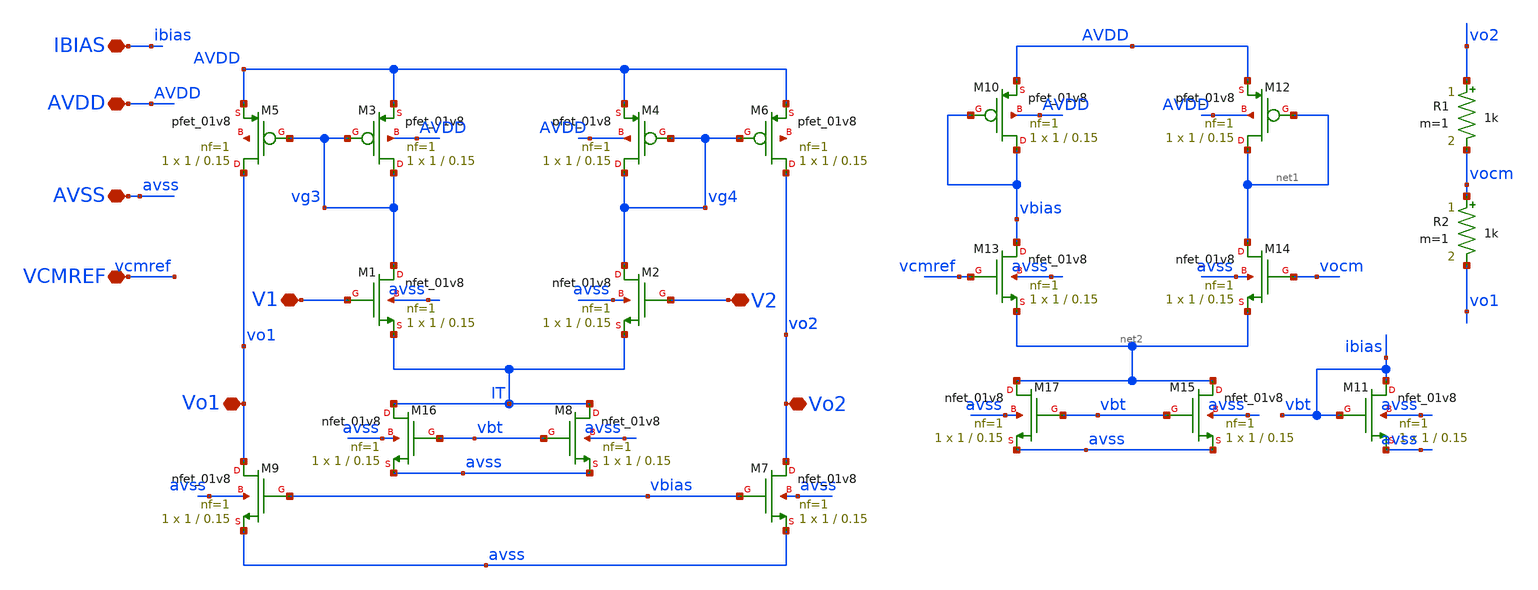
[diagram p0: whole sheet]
** sch_path: xschem/INA/ota_fully_diff.sch
**.subckt ota_fully_diff IBIAS V1 V2 AVDD Vo1 Vo2 AVSS VCMREF
*.iopin IBIAS
*.iopin V1
*.iopin V2
*.iopin AVDD
*.iopin Vo1
*.iopin Vo2
*.iopin AVSS
*.iopin VCMREF
XM3 vg3 vg3 AVDD AVDD sky130_fd_pr__pfet_01v8 L=0.15 W=1 nf=1 ad='int((nf+1)/2) * W/nf * 0.29' as='int((nf+2)/2) * W/nf * 0.29'
+ pd='2*int((nf+1)/2) * (W/nf + 0.29)' ps='2*int((nf+2)/2) * (W/nf + 0.29)' nrd='0.29 / W' nrs='0.29 / W'
+ sa=0 sb=0 sd=0 mult=1 m=1
XM4 vg4 vg4 AVDD AVDD sky130_fd_pr__pfet_01v8 L=0.15 W=1 nf=1 ad='int((nf+1)/2) * W/nf * 0.29' as='int((nf+2)/2) * W/nf * 0.29'
+ pd='2*int((nf+1)/2) * (W/nf + 0.29)' ps='2*int((nf+2)/2) * (W/nf + 0.29)' nrd='0.29 / W' nrs='0.29 / W'
+ sa=0 sb=0 sd=0 mult=1 m=1
XM5 Vo1 vg3 AVDD net3 sky130_fd_pr__pfet_01v8 L=0.15 W=1 nf=1 ad='int((nf+1)/2) * W/nf * 0.29' as='int((nf+2)/2) * W/nf * 0.29'
+ pd='2*int((nf+1)/2) * (W/nf + 0.29)' ps='2*int((nf+2)/2) * (W/nf + 0.29)' nrd='0.29 / W' nrs='0.29 / W'
+ sa=0 sb=0 sd=0 mult=1 m=1
XM6 Vo2 vg4 AVDD net4 sky130_fd_pr__pfet_01v8 L=0.15 W=1 nf=1 ad='int((nf+1)/2) * W/nf * 0.29' as='int((nf+2)/2) * W/nf * 0.29'
+ pd='2*int((nf+1)/2) * (W/nf + 0.29)' ps='2*int((nf+2)/2) * (W/nf + 0.29)' nrd='0.29 / W' nrs='0.29 / W'
+ sa=0 sb=0 sd=0 mult=1 m=1
XM9 Vo1 vbias avss avss sky130_fd_pr__nfet_01v8 L=0.15 W=1 nf=1 ad='int((nf+1)/2) * W/nf * 0.29' as='int((nf+2)/2) * W/nf * 0.29'
+ pd='2*int((nf+1)/2) * (W/nf + 0.29)' ps='2*int((nf+2)/2) * (W/nf + 0.29)' nrd='0.29 / W' nrs='0.29 / W'
+ sa=0 sb=0 sd=0 mult=1 m=1
XM1 vg3 V1 IT avss sky130_fd_pr__nfet_01v8 L=0.15 W=1 nf=1 ad='int((nf+1)/2) * W/nf * 0.29' as='int((nf+2)/2) * W/nf * 0.29'
+ pd='2*int((nf+1)/2) * (W/nf + 0.29)' ps='2*int((nf+2)/2) * (W/nf + 0.29)' nrd='0.29 / W' nrs='0.29 / W'
+ sa=0 sb=0 sd=0 mult=1 m=1
XM2 vg4 V2 IT avss sky130_fd_pr__nfet_01v8 L=0.15 W=1 nf=1 ad='int((nf+1)/2) * W/nf * 0.29' as='int((nf+2)/2) * W/nf * 0.29'
+ pd='2*int((nf+1)/2) * (W/nf + 0.29)' ps='2*int((nf+2)/2) * (W/nf + 0.29)' nrd='0.29 / W' nrs='0.29 / W'
+ sa=0 sb=0 sd=0 mult=1 m=1
XM7 Vo2 vbias avss avss sky130_fd_pr__nfet_01v8 L=0.15 W=1 nf=1 ad='int((nf+1)/2) * W/nf * 0.29' as='int((nf+2)/2) * W/nf * 0.29'
+ pd='2*int((nf+1)/2) * (W/nf + 0.29)' ps='2*int((nf+2)/2) * (W/nf + 0.29)' nrd='0.29 / W' nrs='0.29 / W'
+ sa=0 sb=0 sd=0 mult=1 m=1
XM8 IT vbt avss avss sky130_fd_pr__nfet_01v8 L=0.15 W=1 nf=1 ad='int((nf+1)/2) * W/nf * 0.29' as='int((nf+2)/2) * W/nf * 0.29'
+ pd='2*int((nf+1)/2) * (W/nf + 0.29)' ps='2*int((nf+2)/2) * (W/nf + 0.29)' nrd='0.29 / W' nrs='0.29 / W'
+ sa=0 sb=0 sd=0 mult=1 m=1
XM11 ibias ibias avss avss sky130_fd_pr__nfet_01v8 L=0.15 W=1 nf=1 ad='int((nf+1)/2) * W/nf * 0.29' as='int((nf+2)/2) * W/nf * 0.29'
+ pd='2*int((nf+1)/2) * (W/nf + 0.29)' ps='2*int((nf+2)/2) * (W/nf + 0.29)' nrd='0.29 / W' nrs='0.29 / W'
+ sa=0 sb=0 sd=0 mult=1 m=1
R1 vo2 vocm 1k m=1
R2 vocm vo1 1k m=1
XM10 vbias vbias AVDD AVDD sky130_fd_pr__pfet_01v8 L=0.15 W=1 nf=1 ad='int((nf+1)/2) * W/nf * 0.29' as='int((nf+2)/2) * W/nf * 0.29'
+ pd='2*int((nf+1)/2) * (W/nf + 0.29)' ps='2*int((nf+2)/2) * (W/nf + 0.29)' nrd='0.29 / W' nrs='0.29 / W'
+ sa=0 sb=0 sd=0 mult=1 m=1
XM12 net1 net1 AVDD AVDD sky130_fd_pr__pfet_01v8 L=0.15 W=1 nf=1 ad='int((nf+1)/2) * W/nf * 0.29' as='int((nf+2)/2) * W/nf * 0.29'
+ pd='2*int((nf+1)/2) * (W/nf + 0.29)' ps='2*int((nf+2)/2) * (W/nf + 0.29)' nrd='0.29 / W' nrs='0.29 / W'
+ sa=0 sb=0 sd=0 mult=1 m=1
XM13 vbias vcmref net2 avss sky130_fd_pr__nfet_01v8 L=0.15 W=1 nf=1 ad='int((nf+1)/2) * W/nf * 0.29'
+ as='int((nf+2)/2) * W/nf * 0.29' pd='2*int((nf+1)/2) * (W/nf + 0.29)' ps='2*int((nf+2)/2) * (W/nf + 0.29)'
+ nrd='0.29 / W' nrs='0.29 / W' sa=0 sb=0 sd=0 mult=1 m=1
XM14 net1 vocm net2 avss sky130_fd_pr__nfet_01v8 L=0.15 W=1 nf=1 ad='int((nf+1)/2) * W/nf * 0.29' as='int((nf+2)/2) * W/nf * 0.29'
+ pd='2*int((nf+1)/2) * (W/nf + 0.29)' ps='2*int((nf+2)/2) * (W/nf + 0.29)' nrd='0.29 / W' nrs='0.29 / W'
+ sa=0 sb=0 sd=0 mult=1 m=1
XM16 IT vbt avss avss sky130_fd_pr__nfet_01v8 L=0.15 W=1 nf=1 ad='int((nf+1)/2) * W/nf * 0.29' as='int((nf+2)/2) * W/nf * 0.29'
+ pd='2*int((nf+1)/2) * (W/nf + 0.29)' ps='2*int((nf+2)/2) * (W/nf + 0.29)' nrd='0.29 / W' nrs='0.29 / W'
+ sa=0 sb=0 sd=0 mult=1 m=1
XM15 net2 vbt avss avss sky130_fd_pr__nfet_01v8 L=0.15 W=1 nf=1 ad='int((nf+1)/2) * W/nf * 0.29' as='int((nf+2)/2) * W/nf * 0.29'
+ pd='2*int((nf+1)/2) * (W/nf + 0.29)' ps='2*int((nf+2)/2) * (W/nf + 0.29)' nrd='0.29 / W' nrs='0.29 / W'
+ sa=0 sb=0 sd=0 mult=1 m=1
XM17 net2 vbt avss avss sky130_fd_pr__nfet_01v8 L=0.15 W=1 nf=1 ad='int((nf+1)/2) * W/nf * 0.29' as='int((nf+2)/2) * W/nf * 0.29'
+ pd='2*int((nf+1)/2) * (W/nf + 0.29)' ps='2*int((nf+2)/2) * (W/nf + 0.29)' nrd='0.29 / W' nrs='0.29 / W'
+ sa=0 sb=0 sd=0 mult=1 m=1
**.ends
.end
